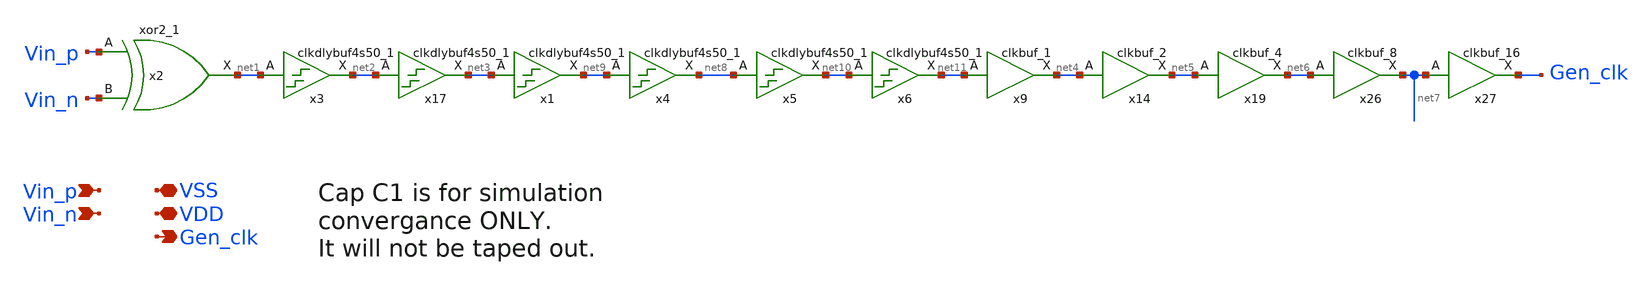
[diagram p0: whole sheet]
** sch_path: xschem/src/xor_clock_gen/xor_clock_gen.sch
**.subckt xor_clock_gen Vin_p VSS Gen_clk VDD Vin_n
*.ipin Vin_p
*.iopin VSS
*.opin Gen_clk
*.iopin VDD
*.ipin Vin_n
x2 Vin_p Vin_n VSS VSS VDD VDD net1 sky130_fd_sc_hd__xor2_1
x3 net1 VSS VSS VDD VDD net2 sky130_fd_sc_hd__clkdlybuf4s50_1
x17 net2 VSS VSS VDD VDD net3 sky130_fd_sc_hd__clkdlybuf4s50_1
x9 net11 VSS VSS VDD VDD net4 sky130_fd_sc_hd__clkbuf_1
x14 net4 VSS VSS VDD VDD net5 sky130_fd_sc_hd__clkbuf_2
x19 net5 VSS VSS VDD VDD net6 sky130_fd_sc_hd__clkbuf_4
x26 net6 VSS VSS VDD VDD net7 sky130_fd_sc_hd__clkbuf_8
x27 net7 VSS VSS VDD VDD Gen_clk sky130_fd_sc_hd__clkbuf_16
x1 net3 VSS VSS VDD VDD net9 sky130_fd_sc_hd__clkdlybuf4s50_1
x4 net9 VSS VSS VDD VDD net8 sky130_fd_sc_hd__clkdlybuf4s50_1
x5 net8 VSS VSS VDD VDD net10 sky130_fd_sc_hd__clkdlybuf4s50_1
x6 net10 VSS VSS VDD VDD net11 sky130_fd_sc_hd__clkdlybuf4s50_1
**.ends
.end
